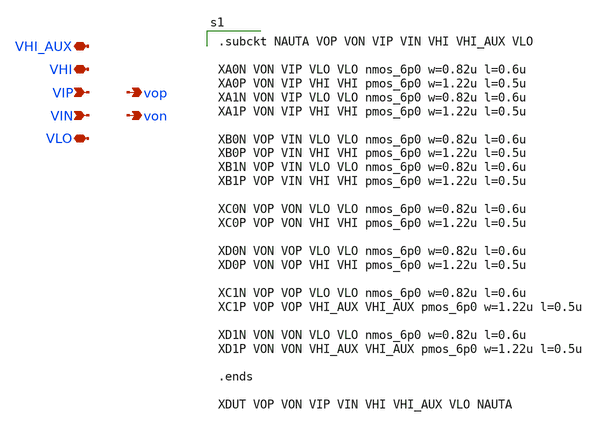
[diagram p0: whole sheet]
** sch_path: xschem/nauta_4.sch
**.subckt nauta_4 VIP VIN vop von VHI VHI_AUX VLO
*.ipin VIP
*.ipin VIN
*.opin vop
*.opin von
*.iopin VHI
*.iopin VHI_AUX
*.iopin VLO
**** begin user architecture code

.subckt NAUTA VOP VON VIP VIN VHI VHI_AUX VLO

XA0N VON VIP VLO VLO nmos_6p0 w=0.82u l=0.6u
XA0P VON VIP VHI VHI pmos_6p0 w=1.22u l=0.5u
XA1N VON VIP VLO VLO nmos_6p0 w=0.82u l=0.6u
XA1P VON VIP VHI VHI pmos_6p0 w=1.22u l=0.5u

XB0N VOP VIN VLO VLO nmos_6p0 w=0.82u l=0.6u
XB0P VOP VIN VHI VHI pmos_6p0 w=1.22u l=0.5u
XB1N VOP VIN VLO VLO nmos_6p0 w=0.82u l=0.6u
XB1P VOP VIN VHI VHI pmos_6p0 w=1.22u l=0.5u

XC0N VOP VON VLO VLO nmos_6p0 w=0.82u l=0.6u
XC0P VOP VON VHI VHI pmos_6p0 w=1.22u l=0.5u

XD0N VON VOP VLO VLO nmos_6p0 w=0.82u l=0.6u
XD0P VON VOP VHI VHI pmos_6p0 w=1.22u l=0.5u

XC1N VOP VOP VLO VLO nmos_6p0 w=0.82u l=0.6u
XC1P VOP VOP VHI_AUX VHI_AUX pmos_6p0 w=1.22u l=0.5u

XD1N VON VON VLO VLO nmos_6p0 w=0.82u l=0.6u
XD1P VON VON VHI_AUX VHI_AUX pmos_6p0 w=1.22u l=0.5u

.ends

XDUT VOP VON VIP VIN VHI VHI_AUX VLO NAUTA


**** end user architecture code
**.ends
.end
